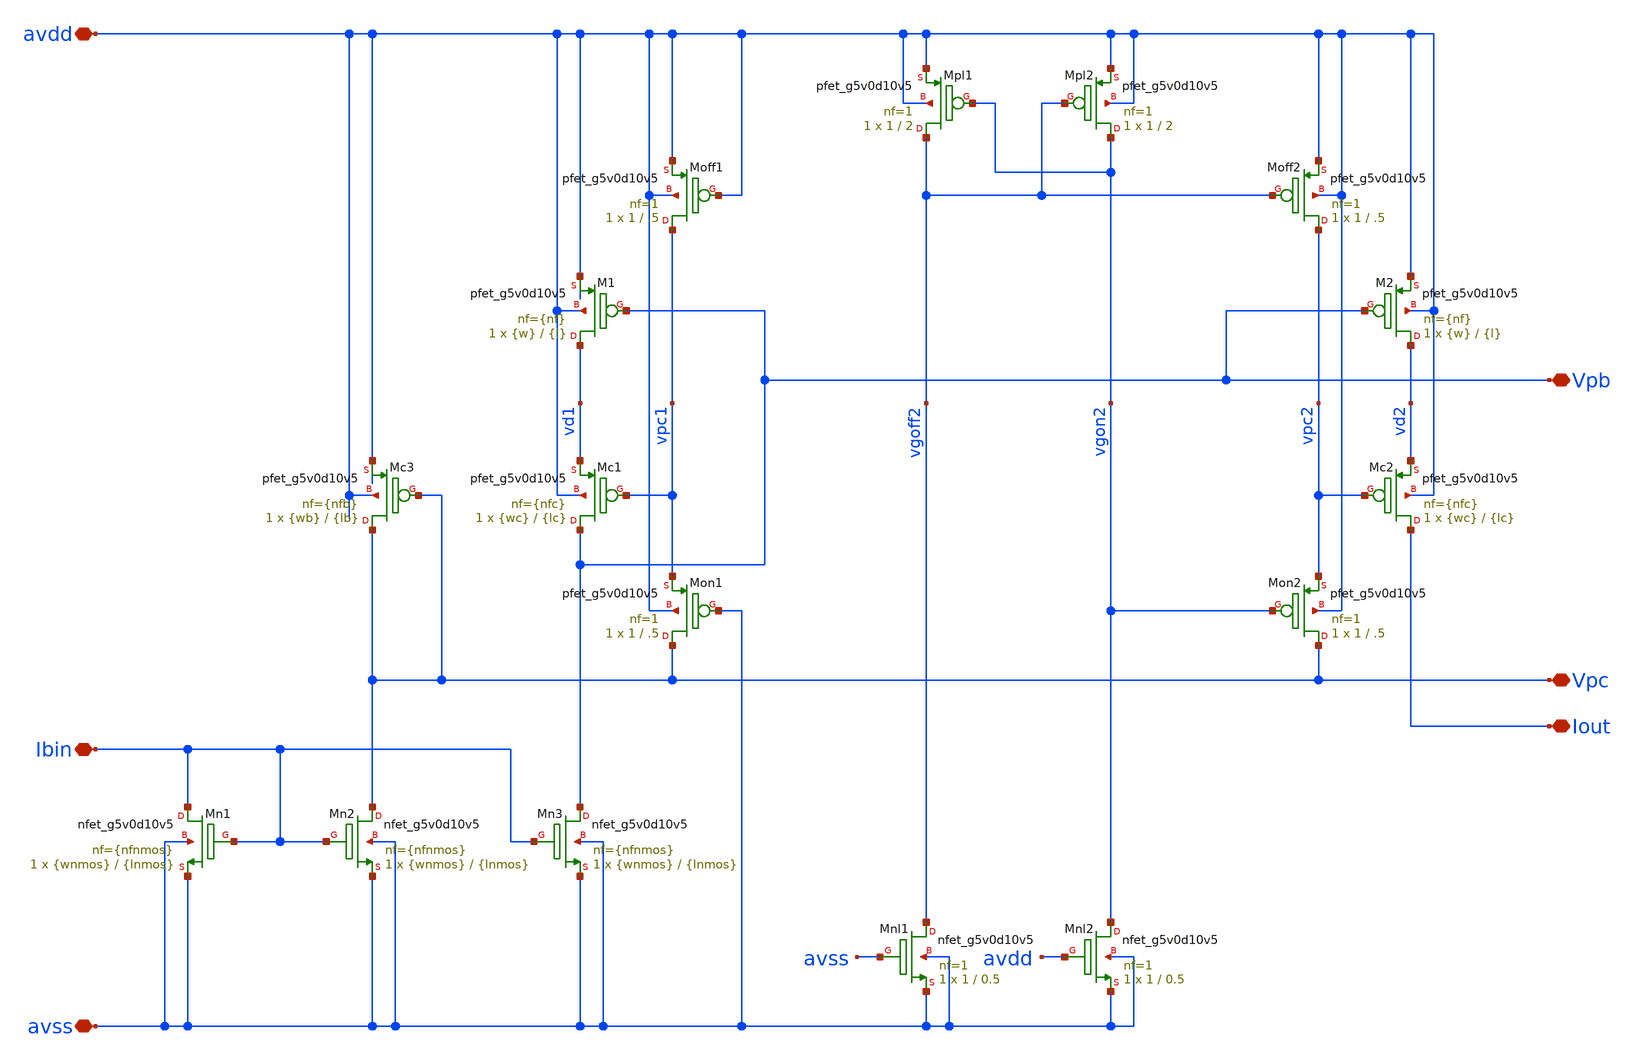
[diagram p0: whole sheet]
** sch_path: xschem/sky130_cm_ip__biasgen.sch
**.subckt sky130_cm_ip__biasgen avss avdd Ibin Vpb Vpc Iout
*.iopin avss
*.iopin avdd
*.iopin Ibin
*.iopin Vpb
*.iopin Vpc
*.iopin Iout
XMc1 Vpb vpc1 vd1 avdd sky130_fd_pr__pfet_g5v0d10v5 L={lc} W={wc} nf={nfc} ad='int(({nfc} + 1)/2) * {wc} / {nfc} * 0.29'
+ as='int(({nfc} + 2)/2) * {wc} / {nfc} * 0.29' pd='2*int(({nfc} + 1)/2) * ({wc} / {nfc} + 0.29)' ps='2*int(({nfc} + 2)/2) * ({wc} / {nfc} + 0.29)'
+ nrd='0.29 / {wc} ' nrs='0.29 / {wc} ' sa=0 sb=0 sd=0 mult=1 m=1
XM1 vd1 Vpb avdd avdd sky130_fd_pr__pfet_g5v0d10v5 L={l} W={w} nf={nf} ad='int(({nf} + 1)/2) * {w} / {nf} * 0.29'
+ as='int(({nf} + 2)/2) * {w} / {nf} * 0.29' pd='2*int(({nf} + 1)/2) * ({w} / {nf} + 0.29)' ps='2*int(({nf} + 2)/2) * ({w} / {nf} + 0.29)'
+ nrd='0.29 / {w} ' nrs='0.29 / {w} ' sa=0 sb=0 sd=0 mult=1 m=1
XMc2 Iout vpc2 vd2 avdd sky130_fd_pr__pfet_g5v0d10v5 L={lc} W={wc} nf={nfc} ad='int(({nfc} + 1)/2) * {wc} / {nfc} * 0.29'
+ as='int(({nfc} + 2)/2) * {wc} / {nfc} * 0.29' pd='2*int(({nfc} + 1)/2) * ({wc} / {nfc} + 0.29)' ps='2*int(({nfc} + 2)/2) * ({wc} / {nfc} + 0.29)'
+ nrd='0.29 / {wc} ' nrs='0.29 / {wc} ' sa=0 sb=0 sd=0 mult=1 m=1
XM2 vd2 Vpb avdd avdd sky130_fd_pr__pfet_g5v0d10v5 L={l} W={w} nf={nf} ad='int(({nf} + 1)/2) * {w} / {nf} * 0.29'
+ as='int(({nf} + 2)/2) * {w} / {nf} * 0.29' pd='2*int(({nf} + 1)/2) * ({w} / {nf} + 0.29)' ps='2*int(({nf} + 2)/2) * ({w} / {nf} + 0.29)'
+ nrd='0.29 / {w} ' nrs='0.29 / {w} ' sa=0 sb=0 sd=0 mult=1 m=1
XMc3 Vpc Vpc avdd avdd sky130_fd_pr__pfet_g5v0d10v5 L={lb} W={wb} nf={nfb} ad='int(({nfb} + 1)/2) * {wb} / {nfb} * 0.29'
+ as='int(({nfb} + 2)/2) * {wb} / {nfb} * 0.29' pd='2*int(({nfb} + 1)/2) * ({wb} / {nfb} + 0.29)' ps='2*int(({nfb} + 2)/2) * ({wb} / {nfb} + 0.29)'
+ nrd='0.29 / {wb} ' nrs='0.29 / {wb} ' sa=0 sb=0 sd=0 mult=1 m=1
XMn1 Ibin Ibin avss avss sky130_fd_pr__nfet_g5v0d10v5 L={lnmos} W={wnmos} nf={nfnmos} ad='int(({nfnmos} + 1)/2) * {wnmos} / {nfnmos} * 0.29'
+ as='int(({nfnmos} + 2)/2) * {wnmos} / {nfnmos} * 0.29' pd='2*int(({nfnmos} + 1)/2) * ({wnmos} / {nfnmos} + 0.29)'
+ ps='2*int(({nfnmos} + 2)/2) * ({wnmos} / {nfnmos} + 0.29)' nrd='0.29 / {wnmos} ' nrs='0.29 / {wnmos} '
+ sa=0 sb=0 sd=0 mult=1 m=1
XMn2 Vpc Ibin avss avss sky130_fd_pr__nfet_g5v0d10v5 L={lnmos} W={wnmos} nf={nfnmos} ad='int(({nfnmos} + 1)/2) * {wnmos} / {nfnmos} * 0.29'
+ as='int(({nfnmos} + 2)/2) * {wnmos} / {nfnmos} * 0.29' pd='2*int(({nfnmos} + 1)/2) * ({wnmos} / {nfnmos} + 0.29)'
+ ps='2*int(({nfnmos} + 2)/2) * ({wnmos} / {nfnmos} + 0.29)' nrd='0.29 / {wnmos} ' nrs='0.29 / {wnmos} '
+ sa=0 sb=0 sd=0 mult=1 m=1
XMn3 Vpb Ibin avss avss sky130_fd_pr__nfet_g5v0d10v5 L={lnmos} W={wnmos} nf={nfnmos} ad='int(({nfnmos} + 1)/2) * {wnmos} / {nfnmos} * 0.29'
+ as='int(({nfnmos} + 2)/2) * {wnmos} / {nfnmos} * 0.29' pd='2*int(({nfnmos} + 1)/2) * ({wnmos} / {nfnmos} + 0.29)'
+ ps='2*int(({nfnmos} + 2)/2) * ({wnmos} / {nfnmos} + 0.29)' nrd='0.29 / {wnmos} ' nrs='0.29 / {wnmos} '
+ sa=0 sb=0 sd=0 mult=1 m=1
XMon1 Vpc avss vpc1 avdd sky130_fd_pr__pfet_g5v0d10v5 L=.5 W=1 nf=1 ad='int((1 + 1)/2) * 1 / 1 * 0.29'
+ as='int((1 + 2)/2) * 1 / 1 * 0.29' pd='2*int((1 + 1)/2) * (1 / 1 + 0.29)' ps='2*int((1 + 2)/2) * (1 / 1 + 0.29)'
+ nrd='0.29 / 1 ' nrs='0.29 / 1 ' sa=0 sb=0 sd=0 mult=1 m=1
XMoff1 vpc1 avdd avdd avdd sky130_fd_pr__pfet_g5v0d10v5 L=.5 W=1 nf=1 ad='int((1 + 1)/2) * 1 / 1 * 0.29'
+ as='int((1 + 2)/2) * 1 / 1 * 0.29' pd='2*int((1 + 1)/2) * (1 / 1 + 0.29)' ps='2*int((1 + 2)/2) * (1 / 1 + 0.29)'
+ nrd='0.29 / 1 ' nrs='0.29 / 1 ' sa=0 sb=0 sd=0 mult=1 m=1
XMon2 Vpc vgon2 vpc2 avdd sky130_fd_pr__pfet_g5v0d10v5 L=.5 W=1 nf=1 ad='int((1 + 1)/2) * 1 / 1 * 0.29'
+ as='int((1 + 2)/2) * 1 / 1 * 0.29' pd='2*int((1 + 1)/2) * (1 / 1 + 0.29)' ps='2*int((1 + 2)/2) * (1 / 1 + 0.29)'
+ nrd='0.29 / 1 ' nrs='0.29 / 1 ' sa=0 sb=0 sd=0 mult=1 m=1
XMoff2 vpc2 vgoff2 avdd avdd sky130_fd_pr__pfet_g5v0d10v5 L=.5 W=1 nf=1 ad='int((1 + 1)/2) * 1 / 1 * 0.29'
+ as='int((1 + 2)/2) * 1 / 1 * 0.29' pd='2*int((1 + 1)/2) * (1 / 1 + 0.29)' ps='2*int((1 + 2)/2) * (1 / 1 + 0.29)'
+ nrd='0.29 / 1 ' nrs='0.29 / 1 ' sa=0 sb=0 sd=0 mult=1 m=1
XMnl1 vgoff2 avss avss avss sky130_fd_pr__nfet_g5v0d10v5 L=0.5 W=1 nf=1 ad='int((1 + 1)/2) * 1 / 1 * 0.29'
+ as='int((1 + 2)/2) * 1 / 1 * 0.29' pd='2*int((1 + 1)/2) * (1 / 1 + 0.29)' ps='2*int((1 + 2)/2) * (1 / 1 + 0.29)'
+ nrd='0.29 / 1 ' nrs='0.29 / 1 ' sa=0 sb=0 sd=0 mult=1 m=1
XMnl2 vgon2 avdd avss avss sky130_fd_pr__nfet_g5v0d10v5 L=0.5 W=1 nf=1 ad='int((1 + 1)/2) * 1 / 1 * 0.29'
+ as='int((1 + 2)/2) * 1 / 1 * 0.29' pd='2*int((1 + 1)/2) * (1 / 1 + 0.29)' ps='2*int((1 + 2)/2) * (1 / 1 + 0.29)'
+ nrd='0.29 / 1 ' nrs='0.29 / 1 ' sa=0 sb=0 sd=0 mult=1 m=1
XMpl1 vgoff2 vgon2 avdd avdd sky130_fd_pr__pfet_g5v0d10v5 L=2 W=1 nf=1 ad='int((1 + 1)/2) * 1 / 1 * 0.29'
+ as='int((1 + 2)/2) * 1 / 1 * 0.29' pd='2*int((1 + 1)/2) * (1 / 1 + 0.29)' ps='2*int((1 + 2)/2) * (1 / 1 + 0.29)'
+ nrd='0.29 / 1 ' nrs='0.29 / 1 ' sa=0 sb=0 sd=0 mult=1 m=1
XMpl2 vgon2 vgoff2 avdd avdd sky130_fd_pr__pfet_g5v0d10v5 L=2 W=1 nf=1 ad='int((1 + 1)/2) * 1 / 1 * 0.29'
+ as='int((1 + 2)/2) * 1 / 1 * 0.29' pd='2*int((1 + 1)/2) * (1 / 1 + 0.29)' ps='2*int((1 + 2)/2) * (1 / 1 + 0.29)'
+ nrd='0.29 / 1 ' nrs='0.29 / 1 ' sa=0 sb=0 sd=0 mult=1 m=1
**.ends
.end
